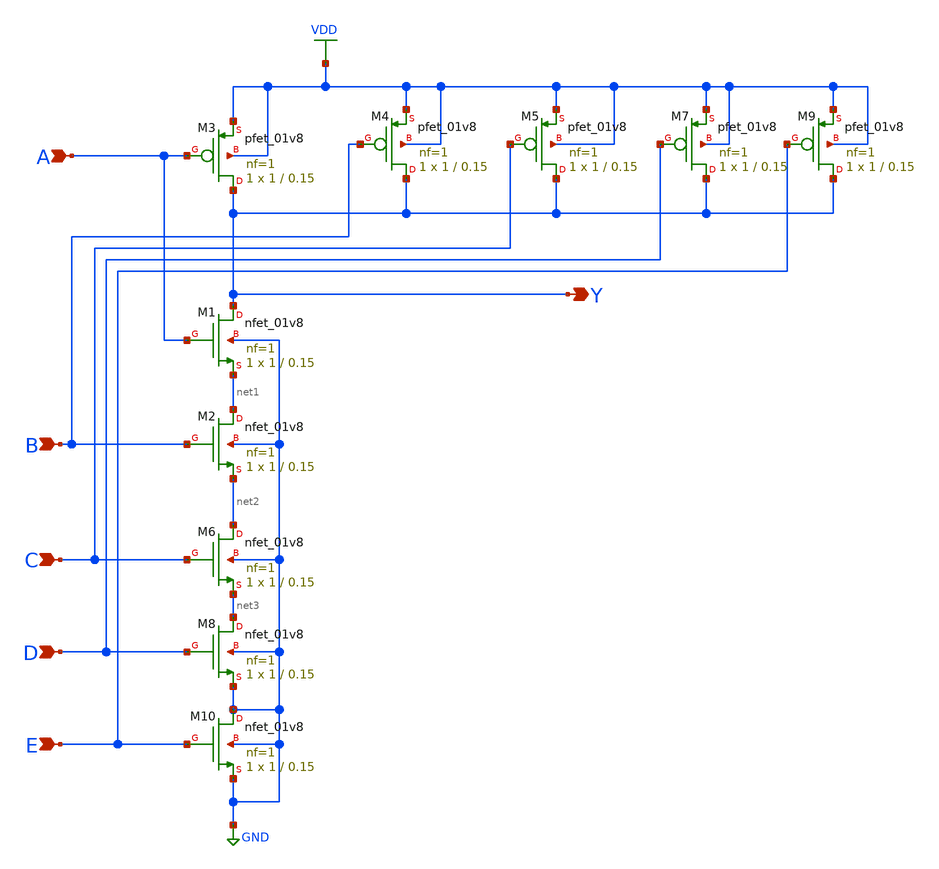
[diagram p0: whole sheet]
** sch_path: gates/NAND5.sch
**.subckt NAND5 A B Y C D E
*.ipin A
*.ipin B
*.opin Y
*.ipin C
*.ipin D
*.ipin E
XM1 Y A net1 GND sky130_fd_pr__nfet_01v8 L=0.15 W=1 nf=1 ad='int((nf+1)/2) * W/nf * 0.29' as='int((nf+2)/2) * W/nf * 0.29'
+ pd='2*int((nf+1)/2) * (W/nf + 0.29)' ps='2*int((nf+2)/2) * (W/nf + 0.29)' nrd='0.29 / W' nrs='0.29 / W'
+ sa=0 sb=0 sd=0 mult=1 m=1
XM2 net1 B net2 GND sky130_fd_pr__nfet_01v8 L=0.15 W=1 nf=1 ad='int((nf+1)/2) * W/nf * 0.29' as='int((nf+2)/2) * W/nf * 0.29'
+ pd='2*int((nf+1)/2) * (W/nf + 0.29)' ps='2*int((nf+2)/2) * (W/nf + 0.29)' nrd='0.29 / W' nrs='0.29 / W'
+ sa=0 sb=0 sd=0 mult=1 m=1
XM3 Y A VDD VDD sky130_fd_pr__pfet_01v8 L=0.15 W=1 nf=1 ad='int((nf+1)/2) * W/nf * 0.29' as='int((nf+2)/2) * W/nf * 0.29'
+ pd='2*int((nf+1)/2) * (W/nf + 0.29)' ps='2*int((nf+2)/2) * (W/nf + 0.29)' nrd='0.29 / W' nrs='0.29 / W'
+ sa=0 sb=0 sd=0 mult=1 m=1
XM4 Y B VDD VDD sky130_fd_pr__pfet_01v8 L=0.15 W=1 nf=1 ad='int((nf+1)/2) * W/nf * 0.29' as='int((nf+2)/2) * W/nf * 0.29'
+ pd='2*int((nf+1)/2) * (W/nf + 0.29)' ps='2*int((nf+2)/2) * (W/nf + 0.29)' nrd='0.29 / W' nrs='0.29 / W'
+ sa=0 sb=0 sd=0 mult=1 m=1
XM5 Y C VDD VDD sky130_fd_pr__pfet_01v8 L=0.15 W=1 nf=1 ad='int((nf+1)/2) * W/nf * 0.29' as='int((nf+2)/2) * W/nf * 0.29'
+ pd='2*int((nf+1)/2) * (W/nf + 0.29)' ps='2*int((nf+2)/2) * (W/nf + 0.29)' nrd='0.29 / W' nrs='0.29 / W'
+ sa=0 sb=0 sd=0 mult=1 m=1
XM6 net2 C net3 GND sky130_fd_pr__nfet_01v8 L=0.15 W=1 nf=1 ad='int((nf+1)/2) * W/nf * 0.29' as='int((nf+2)/2) * W/nf * 0.29'
+ pd='2*int((nf+1)/2) * (W/nf + 0.29)' ps='2*int((nf+2)/2) * (W/nf + 0.29)' nrd='0.29 / W' nrs='0.29 / W'
+ sa=0 sb=0 sd=0 mult=1 m=1
XM7 Y D VDD VDD sky130_fd_pr__pfet_01v8 L=0.15 W=1 nf=1 ad='int((nf+1)/2) * W/nf * 0.29' as='int((nf+2)/2) * W/nf * 0.29'
+ pd='2*int((nf+1)/2) * (W/nf + 0.29)' ps='2*int((nf+2)/2) * (W/nf + 0.29)' nrd='0.29 / W' nrs='0.29 / W'
+ sa=0 sb=0 sd=0 mult=1 m=1
XM8 net3 D GND GND sky130_fd_pr__nfet_01v8 L=0.15 W=1 nf=1 ad='int((nf+1)/2) * W/nf * 0.29' as='int((nf+2)/2) * W/nf * 0.29'
+ pd='2*int((nf+1)/2) * (W/nf + 0.29)' ps='2*int((nf+2)/2) * (W/nf + 0.29)' nrd='0.29 / W' nrs='0.29 / W'
+ sa=0 sb=0 sd=0 mult=1 m=1
XM9 Y E VDD VDD sky130_fd_pr__pfet_01v8 L=0.15 W=1 nf=1 ad='int((nf+1)/2) * W/nf * 0.29' as='int((nf+2)/2) * W/nf * 0.29'
+ pd='2*int((nf+1)/2) * (W/nf + 0.29)' ps='2*int((nf+2)/2) * (W/nf + 0.29)' nrd='0.29 / W' nrs='0.29 / W'
+ sa=0 sb=0 sd=0 mult=1 m=1
XM10 GND E GND GND sky130_fd_pr__nfet_01v8 L=0.15 W=1 nf=1 ad='int((nf+1)/2) * W/nf * 0.29' as='int((nf+2)/2) * W/nf * 0.29'
+ pd='2*int((nf+1)/2) * (W/nf + 0.29)' ps='2*int((nf+2)/2) * (W/nf + 0.29)' nrd='0.29 / W' nrs='0.29 / W'
+ sa=0 sb=0 sd=0 mult=1 m=1
**.ends
.GLOBAL VDD
.GLOBAL GND
.end
